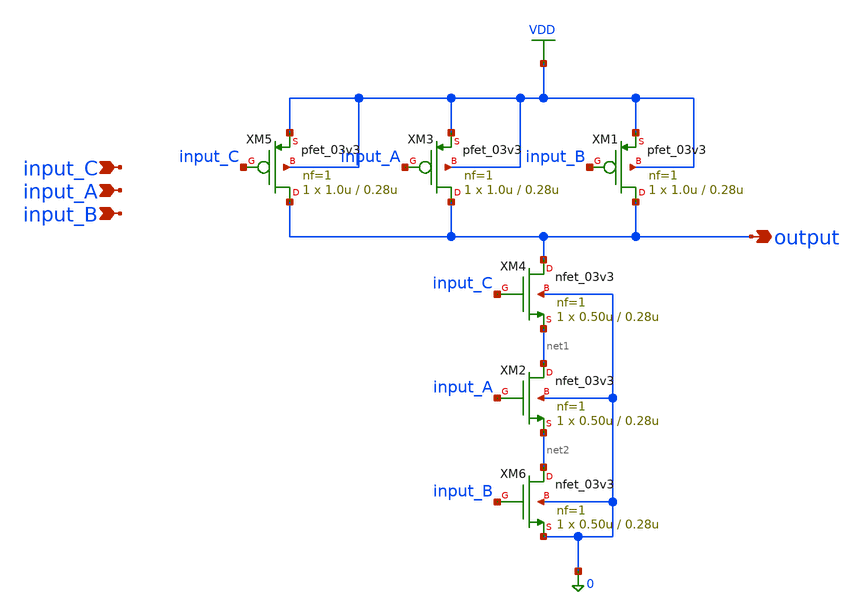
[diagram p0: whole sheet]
** sch_path: xschem/sar_adc/blocks/async_sar/async_nand3.sch
**.subckt async_nand3 input_A input_B input_C output
*.ipin input_A
*.ipin input_B
*.ipin input_C
*.opin output
XM2 net1 input_A net2 0 nfet_03v3 L=0.28u W=0.50u nf=1 ad='int((nf+1)/2) * W/nf * 0.18u' as='int((nf+2)/2) * W/nf * 0.18u'
+ pd='2*int((nf+1)/2) * (W/nf + 0.18u)' ps='2*int((nf+2)/2) * (W/nf + 0.18u)' nrd='0.18u / W' nrs='0.18u / W'
+ sa=0 sb=0 sd=0 m=1
XM3 output input_A VDD VDD pfet_03v3 L=0.28u W=1.0u nf=1 ad='int((nf+1)/2) * W/nf * 0.18u' as='int((nf+2)/2) * W/nf * 0.18u'
+ pd='2*int((nf+1)/2) * (W/nf + 0.18u)' ps='2*int((nf+2)/2) * (W/nf + 0.18u)' nrd='0.18u / W' nrs='0.18u / W'
+ sa=0 sb=0 sd=0 m=1
XM1 output input_B VDD VDD pfet_03v3 L=0.28u W=1.0u nf=1 ad='int((nf+1)/2) * W/nf * 0.18u' as='int((nf+2)/2) * W/nf * 0.18u'
+ pd='2*int((nf+1)/2) * (W/nf + 0.18u)' ps='2*int((nf+2)/2) * (W/nf + 0.18u)' nrd='0.18u / W' nrs='0.18u / W'
+ sa=0 sb=0 sd=0 m=1
XM4 output input_C net1 0 nfet_03v3 L=0.28u W=0.50u nf=1 ad='int((nf+1)/2) * W/nf * 0.18u' as='int((nf+2)/2) * W/nf * 0.18u'
+ pd='2*int((nf+1)/2) * (W/nf + 0.18u)' ps='2*int((nf+2)/2) * (W/nf + 0.18u)' nrd='0.18u / W' nrs='0.18u / W'
+ sa=0 sb=0 sd=0 m=1
XM5 output input_C VDD VDD pfet_03v3 L=0.28u W=1.0u nf=1 ad='int((nf+1)/2) * W/nf * 0.18u' as='int((nf+2)/2) * W/nf * 0.18u'
+ pd='2*int((nf+1)/2) * (W/nf + 0.18u)' ps='2*int((nf+2)/2) * (W/nf + 0.18u)' nrd='0.18u / W' nrs='0.18u / W'
+ sa=0 sb=0 sd=0 m=1
XM6 net2 input_B 0 0 nfet_03v3 L=0.28u W=0.50u nf=1 ad='int((nf+1)/2) * W/nf * 0.18u' as='int((nf+2)/2) * W/nf * 0.18u'
+ pd='2*int((nf+1)/2) * (W/nf + 0.18u)' ps='2*int((nf+2)/2) * (W/nf + 0.18u)' nrd='0.18u / W' nrs='0.18u / W'
+ sa=0 sb=0 sd=0 m=1
**.ends
.GLOBAL VDD
.end
